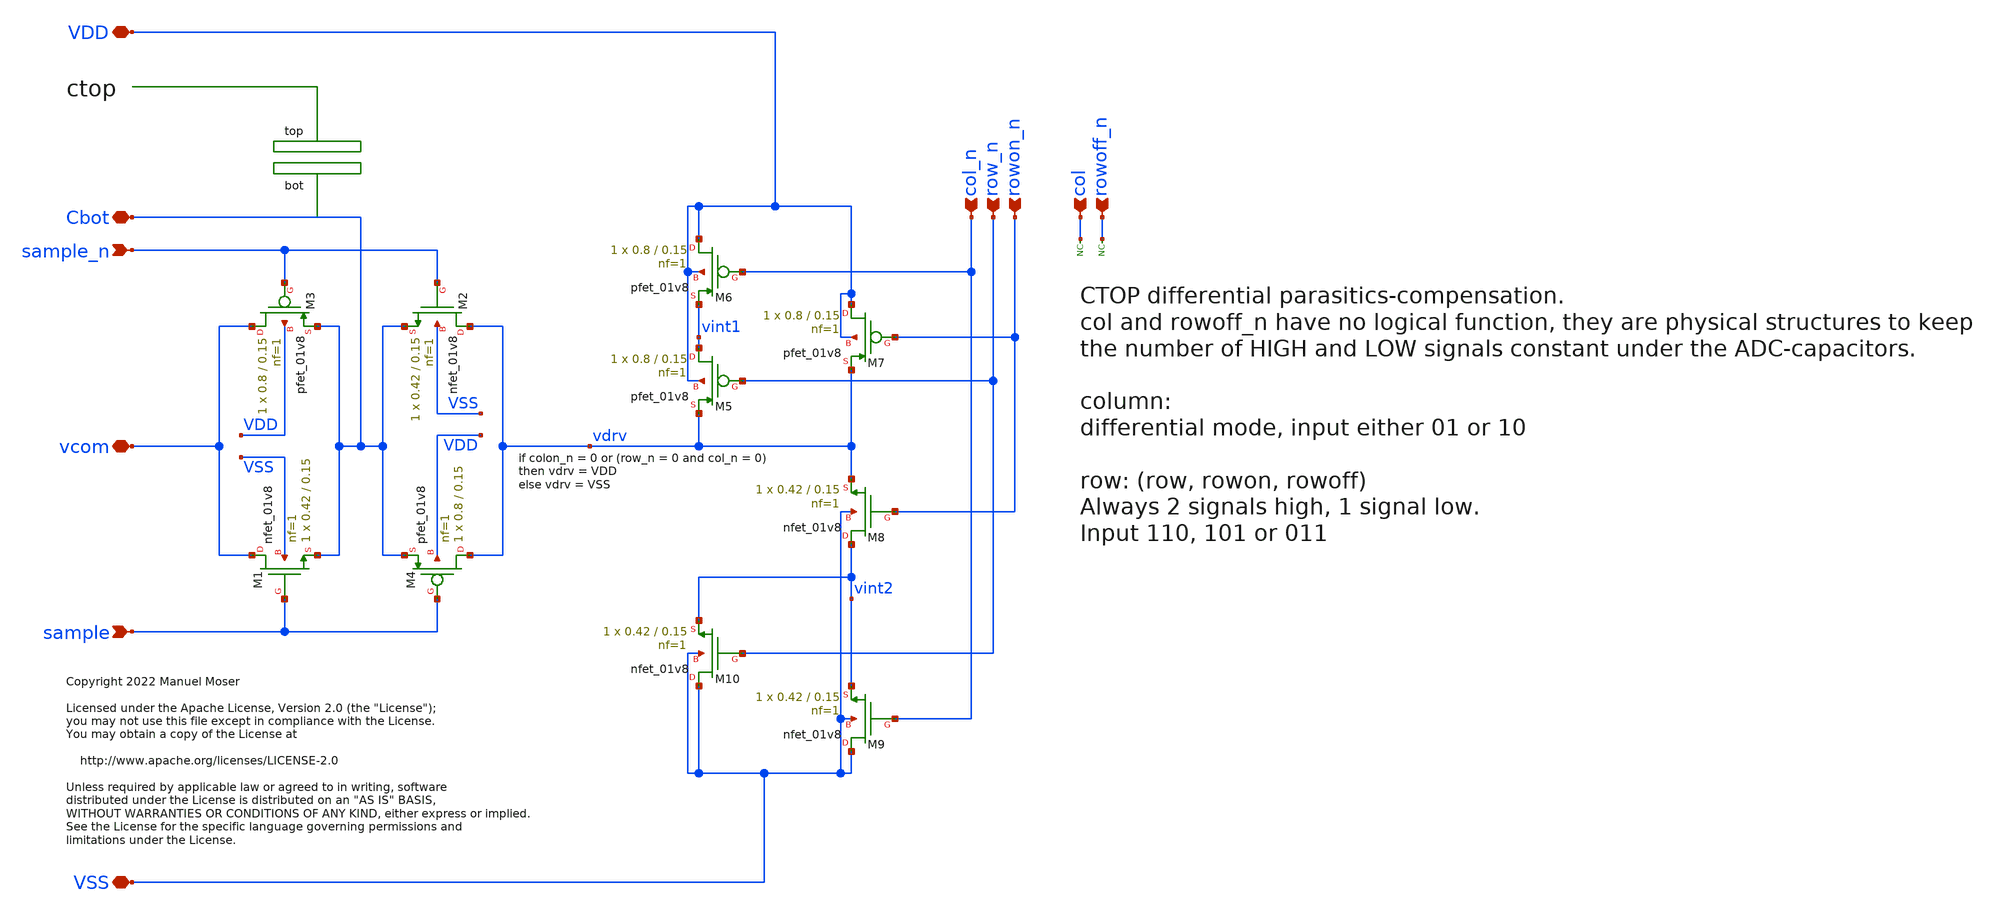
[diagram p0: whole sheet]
** sch_path: xschem/adc_array_circuit_8.sch
* Copyright 2022 Manuel Moser
* Licensed under the Apache License, Version 2.0 (the "License");
**.subckt adc_array_circuit_8 sample_n sample vcom col_n row_n rowon_n VDD VSS Cbot col rowoff_n
*.ipin sample_n
*.ipin sample
*.iopin vcom
*.ipin col_n
*.ipin row_n
*.ipin rowon_n
*.iopin VDD
*.iopin VSS
*.iopin Cbot
*.ipin col
*.ipin rowoff_n
XM1 vcom sample Cbot VSS sky130_fd_pr__nfet_01v8 L=0.15 W=0.42 nf=1 ad='int((nf+1)/2) * W/nf * 0.29'
+ as='int((nf+2)/2) * W/nf * 0.29' pd='2*int((nf+1)/2) * (W/nf + 0.29)' ps='2*int((nf+2)/2) * (W/nf + 0.29)'
+ nrd='0.29 / W' nrs='0.29 / W' sa=0 sb=0 sd=0 mult=1 m=1
XM3 vcom sample_n Cbot VDD sky130_fd_pr__pfet_01v8 L=0.15 W=0.8 nf=1 ad='int((nf+1)/2) * W/nf * 0.29'
+ as='int((nf+2)/2) * W/nf * 0.29' pd='2*int((nf+1)/2) * (W/nf + 0.29)' ps='2*int((nf+2)/2) * (W/nf + 0.29)'
+ nrd='0.29 / W' nrs='0.29 / W' sa=0 sb=0 sd=0 mult=1 m=1
XM2 vdrv sample_n Cbot VSS sky130_fd_pr__nfet_01v8 L=0.15 W=0.42 nf=1 ad='int((nf+1)/2) * W/nf * 0.29'
+ as='int((nf+2)/2) * W/nf * 0.29' pd='2*int((nf+1)/2) * (W/nf + 0.29)' ps='2*int((nf+2)/2) * (W/nf + 0.29)'
+ nrd='0.29 / W' nrs='0.29 / W' sa=0 sb=0 sd=0 mult=1 m=1
XM4 vdrv sample Cbot VDD sky130_fd_pr__pfet_01v8 L=0.15 W=0.8 nf=1 ad='int((nf+1)/2) * W/nf * 0.29' as='int((nf+2)/2) * W/nf * 0.29'
+ pd='2*int((nf+1)/2) * (W/nf + 0.29)' ps='2*int((nf+2)/2) * (W/nf + 0.29)' nrd='0.29 / W' nrs='0.29 / W'
+ sa=0 sb=0 sd=0 mult=1 m=1
XM5 vint1 row_n vdrv VDD sky130_fd_pr__pfet_01v8 L=0.15 W=0.8 nf=1 ad='int((nf+1)/2) * W/nf * 0.29' as='int((nf+2)/2) * W/nf * 0.29'
+ pd='2*int((nf+1)/2) * (W/nf + 0.29)' ps='2*int((nf+2)/2) * (W/nf + 0.29)' nrd='0.29 / W' nrs='0.29 / W'
+ sa=0 sb=0 sd=0 mult=1 m=1
XM6 VDD col_n vint1 VDD sky130_fd_pr__pfet_01v8 L=0.15 W=0.8 nf=1 ad='int((nf+1)/2) * W/nf * 0.29' as='int((nf+2)/2) * W/nf * 0.29'
+ pd='2*int((nf+1)/2) * (W/nf + 0.29)' ps='2*int((nf+2)/2) * (W/nf + 0.29)' nrd='0.29 / W' nrs='0.29 / W'
+ sa=0 sb=0 sd=0 mult=1 m=1
XM7 VDD rowon_n vdrv VDD sky130_fd_pr__pfet_01v8 L=0.15 W=0.8 nf=1 ad='int((nf+1)/2) * W/nf * 0.29' as='int((nf+2)/2) * W/nf * 0.29'
+ pd='2*int((nf+1)/2) * (W/nf + 0.29)' ps='2*int((nf+2)/2) * (W/nf + 0.29)' nrd='0.29 / W' nrs='0.29 / W'
+ sa=0 sb=0 sd=0 mult=1 m=1
XM8 vint2 rowon_n vdrv VSS sky130_fd_pr__nfet_01v8 L=0.15 W=0.42 nf=1 ad='int((nf+1)/2) * W/nf * 0.29'
+ as='int((nf+2)/2) * W/nf * 0.29' pd='2*int((nf+1)/2) * (W/nf + 0.29)' ps='2*int((nf+2)/2) * (W/nf + 0.29)'
+ nrd='0.29 / W' nrs='0.29 / W' sa=0 sb=0 sd=0 mult=1 m=1
XM9 VSS col_n vint2 VSS sky130_fd_pr__nfet_01v8 L=0.15 W=0.42 nf=1 ad='int((nf+1)/2) * W/nf * 0.29' as='int((nf+2)/2) * W/nf * 0.29'
+ pd='2*int((nf+1)/2) * (W/nf + 0.29)' ps='2*int((nf+2)/2) * (W/nf + 0.29)' nrd='0.29 / W' nrs='0.29 / W'
+ sa=0 sb=0 sd=0 mult=1 m=1
XM10 VSS row_n vint2 VSS sky130_fd_pr__nfet_01v8 L=0.15 W=0.42 nf=1 ad='int((nf+1)/2) * W/nf * 0.29'
+ as='int((nf+2)/2) * W/nf * 0.29' pd='2*int((nf+1)/2) * (W/nf + 0.29)' ps='2*int((nf+2)/2) * (W/nf + 0.29)'
+ nrd='0.29 / W' nrs='0.29 / W' sa=0 sb=0 sd=0 mult=1 m=1
* noconn col
* noconn rowoff_n
**.ends
.end
